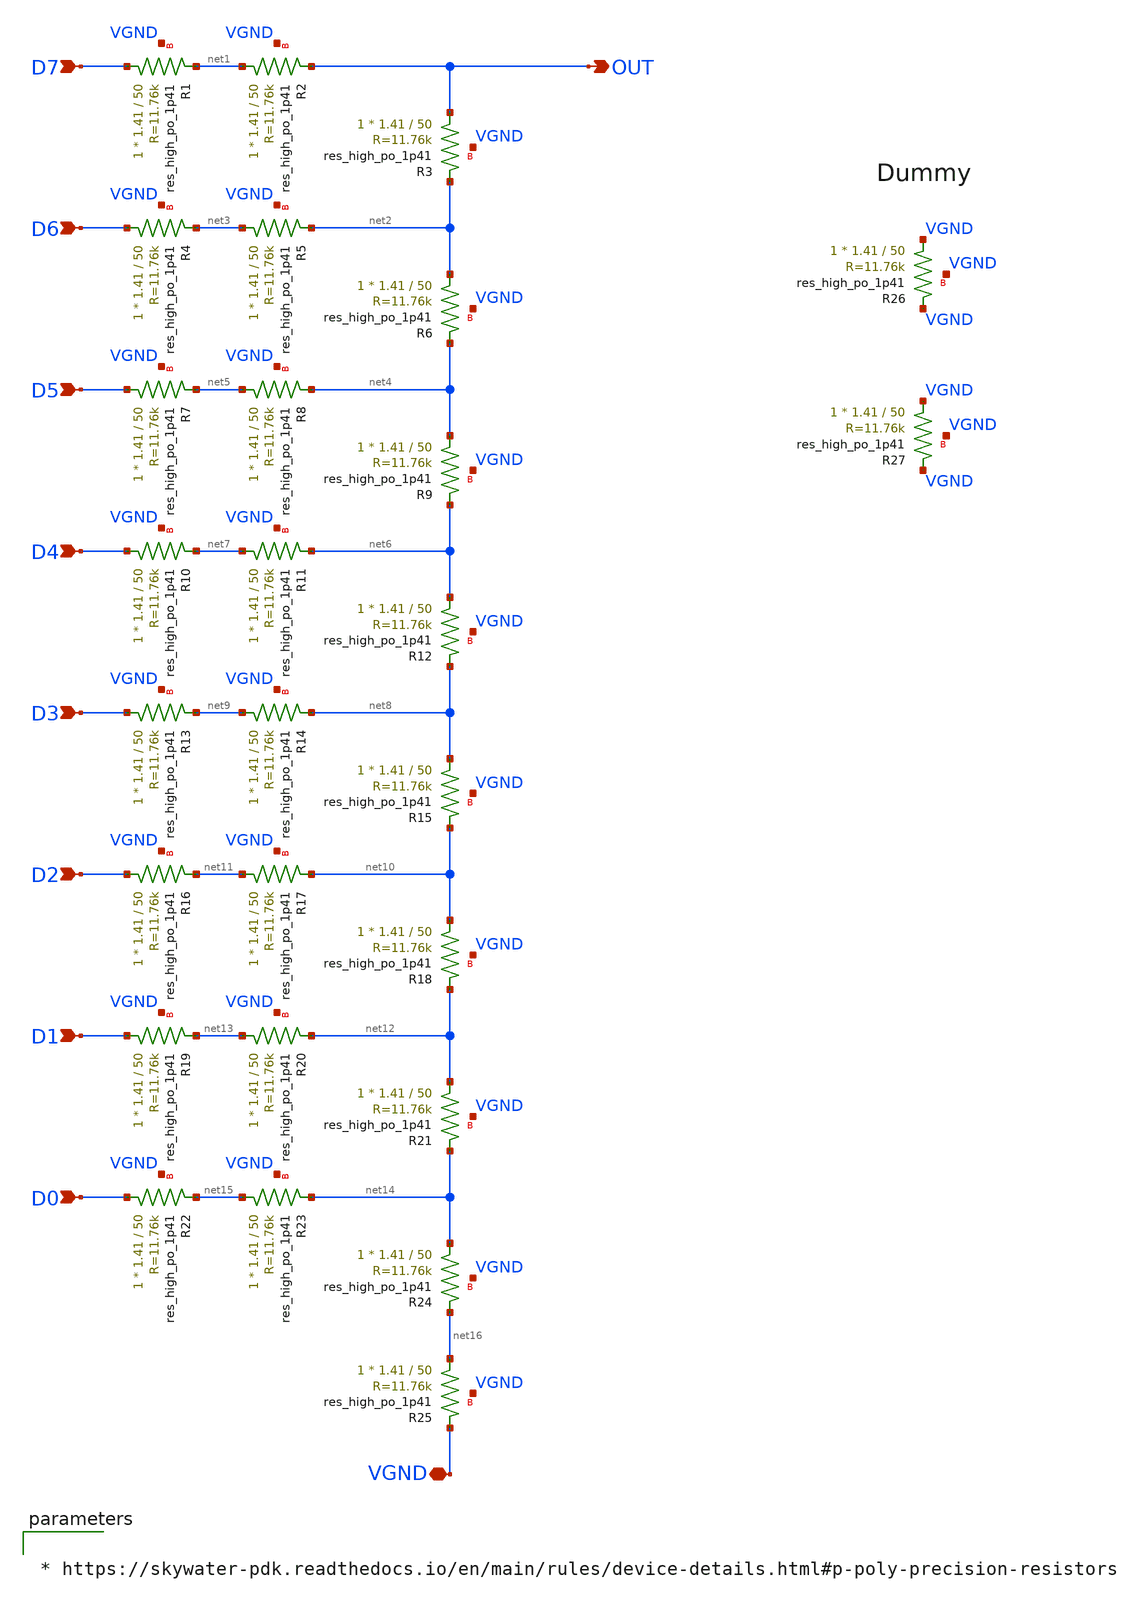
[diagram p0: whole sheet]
** sch_path: xschem/sky130_leo_ip__rdac_8bit.sch
**.subckt sky130_leo_ip__rdac_8bit VGND D7 D6 D5 D4 D3 D2 D1 D0 OUT
*.iopin VGND
*.ipin D7
*.ipin D6
*.ipin D5
*.ipin D4
*.ipin D3
*.ipin D2
*.ipin D1
*.ipin D0
*.opin OUT
XR1 D7 net1 VGND sky130_fd_pr__res_high_po_1p41 L=50 mult=1 m=1
XR2 net1 OUT VGND sky130_fd_pr__res_high_po_1p41 L=50 mult=1 m=1
XR3 OUT net2 VGND sky130_fd_pr__res_high_po_1p41 L=50 mult=1 m=1
XR4 D6 net3 VGND sky130_fd_pr__res_high_po_1p41 L=50 mult=1 m=1
XR5 net3 net2 VGND sky130_fd_pr__res_high_po_1p41 L=50 mult=1 m=1
XR6 net2 net4 VGND sky130_fd_pr__res_high_po_1p41 L=50 mult=1 m=1
XR7 D5 net5 VGND sky130_fd_pr__res_high_po_1p41 L=50 mult=1 m=1
XR8 net5 net4 VGND sky130_fd_pr__res_high_po_1p41 L=50 mult=1 m=1
XR9 net4 net6 VGND sky130_fd_pr__res_high_po_1p41 L=50 mult=1 m=1
XR10 D4 net7 VGND sky130_fd_pr__res_high_po_1p41 L=50 mult=1 m=1
XR11 net7 net6 VGND sky130_fd_pr__res_high_po_1p41 L=50 mult=1 m=1
XR12 net6 net8 VGND sky130_fd_pr__res_high_po_1p41 L=50 mult=1 m=1
XR13 D3 net9 VGND sky130_fd_pr__res_high_po_1p41 L=50 mult=1 m=1
XR14 net9 net8 VGND sky130_fd_pr__res_high_po_1p41 L=50 mult=1 m=1
XR15 net8 net10 VGND sky130_fd_pr__res_high_po_1p41 L=50 mult=1 m=1
XR16 D2 net11 VGND sky130_fd_pr__res_high_po_1p41 L=50 mult=1 m=1
XR17 net11 net10 VGND sky130_fd_pr__res_high_po_1p41 L=50 mult=1 m=1
XR18 net10 net12 VGND sky130_fd_pr__res_high_po_1p41 L=50 mult=1 m=1
XR19 D1 net13 VGND sky130_fd_pr__res_high_po_1p41 L=50 mult=1 m=1
XR20 net13 net12 VGND sky130_fd_pr__res_high_po_1p41 L=50 mult=1 m=1
XR21 net12 net14 VGND sky130_fd_pr__res_high_po_1p41 L=50 mult=1 m=1
XR22 D0 net15 VGND sky130_fd_pr__res_high_po_1p41 L=50 mult=1 m=1
XR23 net15 net14 VGND sky130_fd_pr__res_high_po_1p41 L=50 mult=1 m=1
XR24 net14 net16 VGND sky130_fd_pr__res_high_po_1p41 L=50 mult=1 m=1
XR25 net16 VGND VGND sky130_fd_pr__res_high_po_1p41 L=50 mult=1 m=1
XR26 VGND VGND VGND sky130_fd_pr__res_high_po_1p41 L=50 mult=1 m=1
XR27 VGND VGND VGND sky130_fd_pr__res_high_po_1p41 L=50 mult=1 m=1
**** begin user architecture code


* https://skywater-pdk.readthedocs.io/en/main/rules/device-details.html#p-poly-precision-resistors


**** end user architecture code
**.ends
.end
